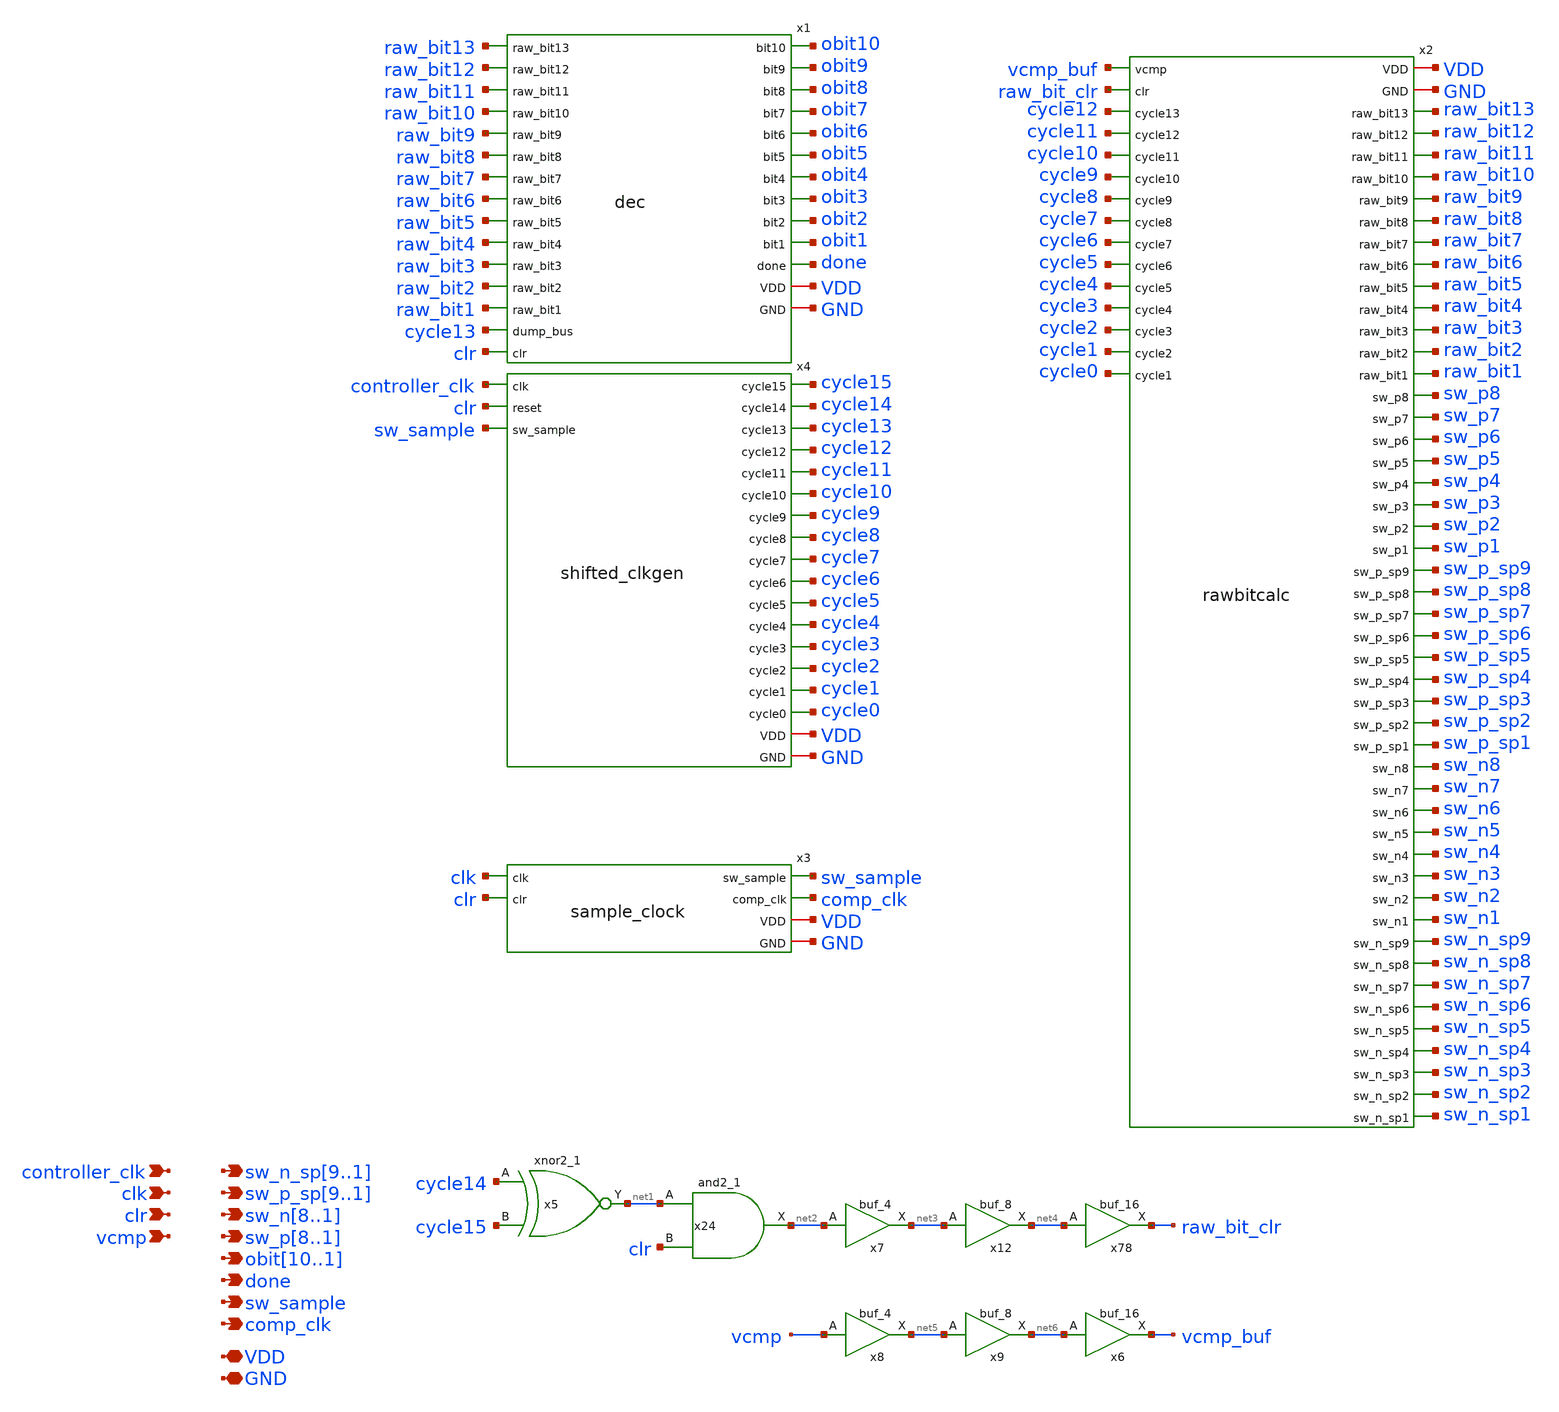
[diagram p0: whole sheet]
** sch_path: xschem/controller/controller.sch
**.subckt controller clk vcmp VDD GND clr controller_clk
*+ sw_n_sp9,sw_n_sp8,sw_n_sp7,sw_n_sp6,sw_n_sp5,sw_n_sp4,sw_n_sp3,sw_n_sp2,sw_n_sp1 sw_p_sp9,sw_p_sp8,sw_p_sp7,sw_p_sp6,sw_p_sp5,sw_p_sp4,sw_p_sp3,sw_p_sp2,sw_p_sp1
*+ sw_p8,sw_p7,sw_p6,sw_p5,sw_p4,sw_p3,sw_p2,sw_p1 sw_n8,sw_n7,sw_n6,sw_n5,sw_n4,sw_n3,sw_n2,sw_n1
*+ obit10,obit9,obit8,obit7,obit6,obit5,obit4,obit3,obit2,obit1 done sw_sample comp_clk
*.ipin clk
*.ipin vcmp
*.iopin VDD
*.iopin GND
*.ipin clr
*.ipin controller_clk
*.opin sw_n_sp9,sw_n_sp8,sw_n_sp7,sw_n_sp6,sw_n_sp5,sw_n_sp4,sw_n_sp3,sw_n_sp2,sw_n_sp1
*.opin sw_p_sp9,sw_p_sp8,sw_p_sp7,sw_p_sp6,sw_p_sp5,sw_p_sp4,sw_p_sp3,sw_p_sp2,sw_p_sp1
*.opin sw_p8,sw_p7,sw_p6,sw_p5,sw_p4,sw_p3,sw_p2,sw_p1
*.opin sw_n8,sw_n7,sw_n6,sw_n5,sw_n4,sw_n3,sw_n2,sw_n1
*.opin obit10,obit9,obit8,obit7,obit6,obit5,obit4,obit3,obit2,obit1
*.opin done
*.opin sw_sample
*.opin comp_clk
x5 cycle14 cycle15 GND GND VDD VDD net1 sky130_fd_sc_hd__xnor2_1
x24 net1 clr GND GND VDD VDD net2 sky130_fd_sc_hd__and2_1
x78 net4 GND GND VDD VDD raw_bit_clr sky130_fd_sc_hd__buf_16
x7 net2 GND GND VDD VDD net3 sky130_fd_sc_hd__buf_4
x12 net3 GND GND VDD VDD net4 sky130_fd_sc_hd__buf_8
x6 net6 GND GND VDD VDD vcmp_buf sky130_fd_sc_hd__buf_16
x8 vcmp GND GND VDD VDD net5 sky130_fd_sc_hd__buf_4
x9 net5 GND GND VDD VDD net6 sky130_fd_sc_hd__buf_8
x1 obit10 raw_bit13 raw_bit12 obit9 raw_bit11 obit8 obit7 raw_bit10 obit6 raw_bit9 raw_bit8 obit5
+ obit4 raw_bit7 raw_bit6 obit3 obit2 raw_bit5 raw_bit4 obit1 raw_bit3 done raw_bit2 raw_bit1 VDD cycle13
+ GND clr dec
x2 VDD vcmp_buf GND raw_bit_clr cycle12 raw_bit13 raw_bit12 cycle11 cycle10 raw_bit11 raw_bit10
+ cycle9 cycle8 raw_bit9 raw_bit8 cycle7 raw_bit7 cycle6 raw_bit6 cycle5 raw_bit5 cycle4 raw_bit4 cycle3
+ raw_bit3 cycle2 raw_bit2 cycle1 cycle0 raw_bit1 sw_p8 sw_p7 sw_p6 sw_p5 sw_p4 sw_p3 sw_p2 sw_p1 sw_p_sp9
+ sw_p_sp8 sw_p_sp7 sw_p_sp6 sw_p_sp5 sw_p_sp4 sw_p_sp3 sw_p_sp2 sw_p_sp1 sw_n8 sw_n7 sw_n6 sw_n5 sw_n4 sw_n3
+ sw_n2 sw_n1 sw_n_sp9 sw_n_sp8 sw_n_sp7 sw_n_sp6 sw_n_sp5 sw_n_sp4 sw_n_sp3 sw_n_sp2 sw_n_sp1 rawbitcalc
x3 sw_sample clk clr comp_clk VDD GND sample_clock
x4 cycle15 cycle14 cycle13 cycle12 controller_clk cycle11 clr cycle10 sw_sample cycle9 cycle8 cycle7
+ cycle6 cycle5 cycle4 cycle3 cycle2 cycle1 cycle0 VDD GND shifted_clkgen
**.ends
.end
